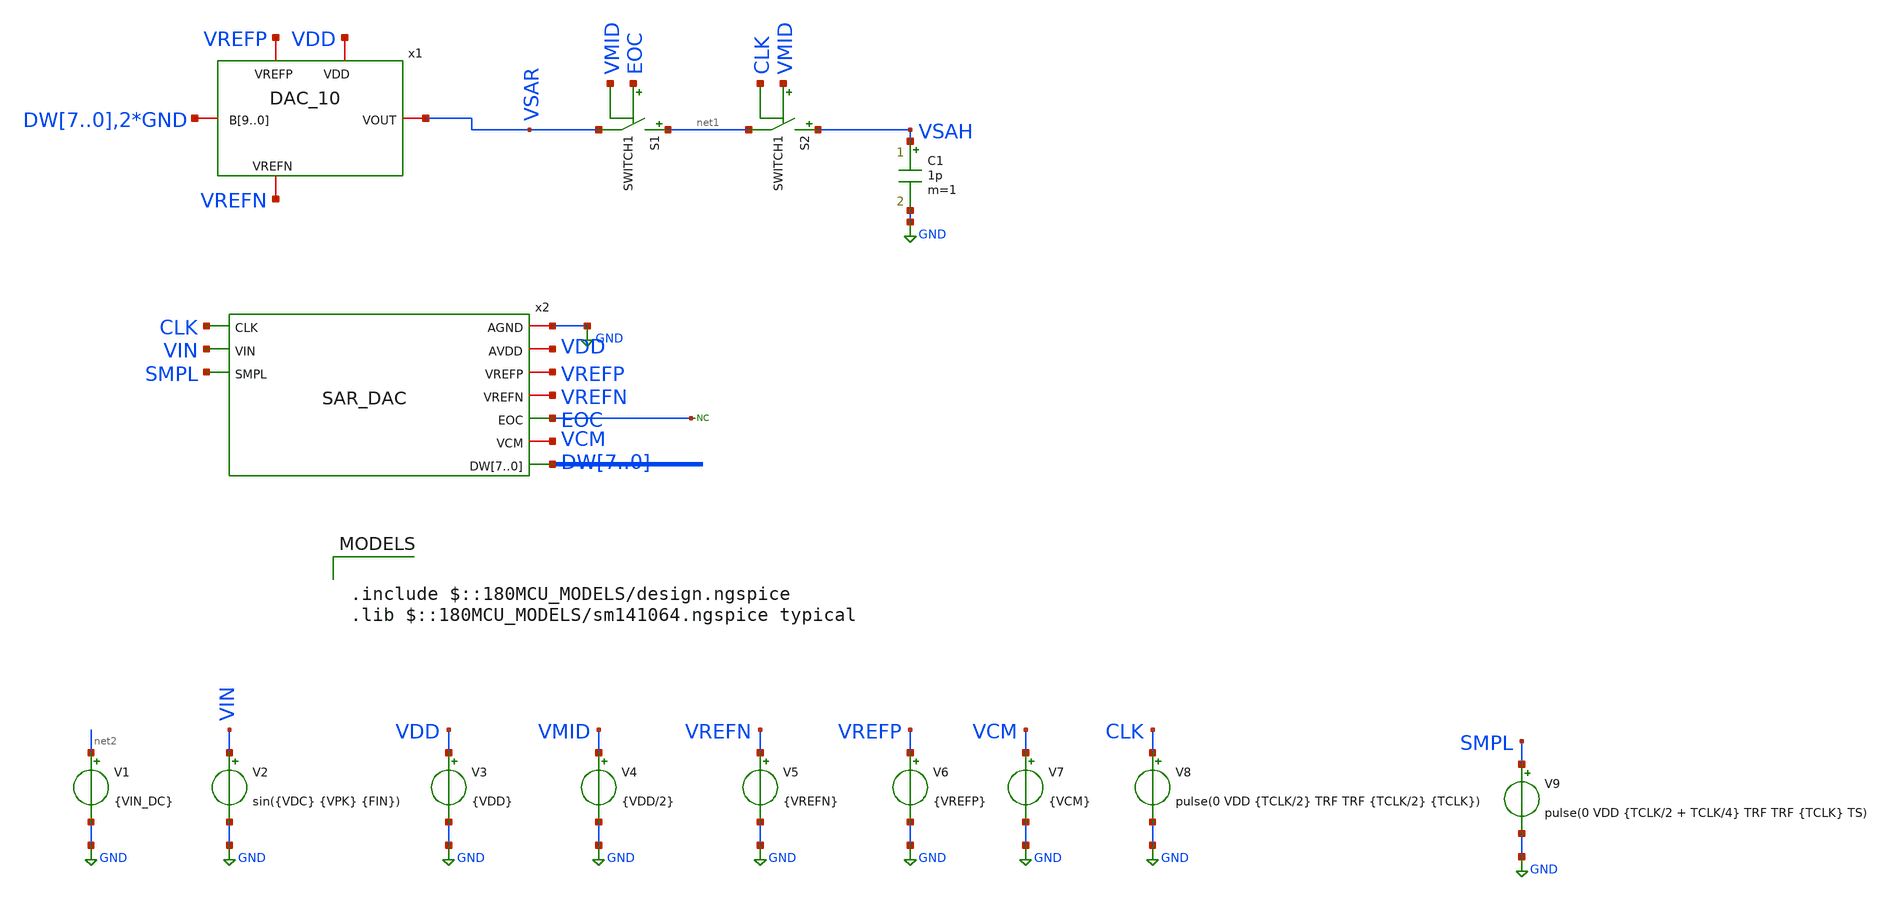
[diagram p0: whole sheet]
** sch_path: XSCHEM Files/final.sch
**.subckt final
S1 net1 VSAR EOC VMID SWITCH1
S2 VSAH net1 VMID CLK SWITCH1
C1 VSAH GND 1p m=1
V1 net2 GND {VIN_DC}
V2 VIN GND sin({VDC} {VPK} {FIN})
V3 VDD GND {VDD}
V4 VMID GND {VDD/2}
V5 VREFN GND {VREFN}
V6 VREFP GND {VREFP}
V7 VCM GND {VCM}
V8 CLK GND pulse(0 VDD {TCLK/2} TRF TRF {TCLK/2} {TCLK})
V9 SMPL GND pulse(0 VDD {TCLK/2 + TCLK/4} TRF TRF {TCLK} TS)
x1 VREFP VDD VSAR DW7 DW6 DW5 DW4 DW3 DW2 DW1 DW0 GND GND VREFN DAC_10
* noconn EOC
x2 GND VDD CLK VIN VREFP VREFN SMPL EOC VCM DW7 DW6 DW5 DW4 DW3 DW2 DW1 DW0 SAR_DAC
**** begin user architecture code

.include $::180MCU_MODELS/design.ngspice
.lib $::180MCU_MODELS/sm141064.ngspice typical



* ngspice commands
*Required model for the switch (the switch threshold default value is zero)
* you can define the threshold using vt={VDD/2} (not needed here)
.model SWITCH1 sw
*These are the values of the parameters to be used
.param TS=1u TCLK=100n TRF=1n TDROP={0.5/FIN} TSTOP={(NCYC/FIN)+TDROP}
.param NCYC=5 NFFT=256 FIN={(NCYC/NFFT)/TS}
.param VDD=3 VDC={1} VCM={1} VPK={0.5} VREFP={VCM+VPK} VREFN={VCM-VPK}
.param VCC=VDD
*.param VIN_DC={VREFN}
*.param VIN_DC={VREFP}
.param VIN_DC= {VREFN +(128+32+8+2+0.5)*2*VPK/(2**8)}
*Analysis setup and control statements
.tran 1n {TSTOP} {TDROP}
*.tran 1n {2*TS}
*save all voltages and currents
.save all
*options for an accurate precision output
*.options reltol=1e-6 vntol=1u abstol=1p
* option to make output file ascii
*.options filetype=ascii


**** end user architecture code
**.ends

* expanding   symbol:  /home/tare/Desktop/Final_1/DAC_10.sym # of pins=5
** sym_path: XSCHEM Files/DAC_10.sym
** sch_path: XSCHEM Files/DAC_10.sch
.subckt DAC_10 VREFP VDD VOUT B9 B8 B7 B6 B5 B4 B3 B2 B1 B0 VREFN
*.iopin B9,B8,B7,B6,B5,B4,B3,B2,B1,B0
*.iopin VREFP
*.iopin VREFN
*.iopin VOUT
*.iopin VDD
x19 VDD BO9 B9 Bitlogic
x18 VDD BO8 B8 Bitlogic
x17 VDD BO7 B7 Bitlogic
x16 VDD BO6 B6 Bitlogic
x15 VDD BO5 B5 Bitlogic
x14 VDD BO4 B4 Bitlogic
x13 VDD BO3 B3 Bitlogic
x12 VDD BO2 B2 Bitlogic
x11 VDD BO1 B1 Bitlogic
x10 VDD BO0 B0 Bitlogic
B1 VOUT GND
+ v=(512*v(BO9)+256*v(BO8)+128*v(BO7)+64*v(BO6)+32*v(BO5)+16*v(BO4)+8*v(BO3)+4*v(BO2)+2*v(BO1)+v(BO0))*((v(VREFP)-v(VREFN))/1024)+v(VREFN)
.ends


* expanding   symbol:  /home/tare/Desktop/last/SAR_DAC.sym # of pins=10
** sym_path: XSCHEM Files/SAR_DAC.sym
** sch_path: XSCHEM Files/SAR_DAC.sch
.subckt SAR_DAC AGND AVDD CLK VIN VREFP VREFN SMPL EOC VCM DW7 DW6 DW5 DW4 DW3 DW2 DW1 DW0
*.iopin AGND
*.iopin AVDD
*.iopin VREFP
*.iopin VREFN
*.iopin VCM
*.ipin VIN
*.ipin SMPL
*.ipin CLK
*.opin EOC
*.opin DW7,DW6,DW5,DW4,DW3,DW2,DW1,DW0
* noconn DW_B[7..0]
* noconn #net1
x8 CMP CLK SMPL DW7 DW6 DW5 DW4 DW3 DW2 DW1 DW0 DW_B7 DW_B6 DW_B5 DW_B4 DW_B3 DW_B2 DW_B1 DW_B0 EOC
+ sar_logic
x2 CMP VCM net1 VDAC comperator
x4 SMPL_B SMPL inv
x5 SMPL_D SMPL_B inv
x6 SMPL_B_D SMPL_D inv
x1 AVDD AGND VREFN VREFP SMPL_B_D DW7 DW6 DW5 DW4 DW3 DW2 DW1 DW0 SMPL_D VREFN VIN VDAC Cap_DAC
x3 SMPL AGND VDAC VCM AVDD tg
.ends


* expanding   symbol:  Bitlogic.sym # of pins=3
** sym_path: XSCHEM Files/Bitlogic.sym
** sch_path: XSCHEM Files/Bitlogic.sch
.subckt Bitlogic VDD BOUT BIN
*.opin BOUT
*.ipin BIN
*.iopin VDD
V1 ONE GND 1
S1 ONE BOUT BIN VMID SWITCH1
S2 BOUT GND VMID BIN SWITCH1
R1 VMID GND 1meg m=1
R2 VDD VMID 1meg m=1
.ends


* expanding   symbol:  /home/tare/Desktop/Final_1/sar_logic.sym # of pins=6
** sym_path: XSCHEM Files/sar_logic.sym
** sch_path: XSCHEM Files/sar_logic.sch
.subckt sar_logic CMP CLK RST DW7 DW6 DW5 DW4 DW3 DW2 DW1 DW0 DW_B7 DW_B6 DW_B5 DW_B4 DW_B3 DW_B2
+ DW_B1 DW_B0 EOC
*.ipin CMP
*.opin DW7,DW6,DW5,DW4,DW3,DW2,DW1,DW0
*.ipin CLK
*.ipin RST
*.opin DW_B7,DW_B6,DW_B5,DW_B4,DW_B3,DW_B2,DW_B1,DW_B0
*.opin EOC
**** begin user architecture code


V1 VLOW 0 0


**** end user architecture code
xRING_CNT8 VLOW CLK RST VLOW QCNT8 Q_B8 dff
xRING_CNT7 QCNT8 CLK VLOW RST QCNT7 Q_B7 dff
xRING_CNT6 QCNT7 CLK VLOW RST QCNT6 Q_B6 dff
xRING_CNT5 QCNT6 CLK VLOW RST QCNT5 Q_B5 dff
xRING_CNT4 QCNT5 CLK VLOW RST QCNT4 Q_B4 dff
xRING_CNT3 QCNT4 CLK VLOW RST QCNT3 Q_B3 dff
xRING_CNT2 QCNT3 CLK VLOW RST QCNT2 Q_B2 dff
xRING_CNT1 QCNT2 CLK VLOW RST QCNT1 Q_B1 dff
xRING_CNT0 QCNT1 CLK VLOW RST QCNT0 Q_B0 dff
xCODE_REG7 CMP DW6 QCNT8 VLOW DW7 DW_B7 dff
xCODE_REG6 CMP DW5 QCNT7 RST DW6 DW_B6 dff
xCODE_REG5 CMP DW4 QCNT6 RST DW5 DW_B5 dff
xCODE_REG4 CMP DW3 QCNT5 RST DW4 DW_B4 dff
xCODE_REG3 CMP DW2 QCNT4 RST DW3 DW_B3 dff
xCODE_REG2 CMP DW1 QCNT3 RST DW2 DW_B2 dff
xCODE_REG1 CMP DW0 QCNT2 RST DW1 DW_B1 dff
xCODE_REG0 CMP EOC QCNT1 RST DW0 DW_B0 dff
x3 VLOW VLOW QCNT0 RST EOC net1 dff
.ends


* expanding   symbol:  /home/tare/Desktop/Final_1/comperator.sym # of pins=4
** sym_path: XSCHEM Files/comperator.sym
** sch_path: XSCHEM Files/comperator.sch
.subckt comperator VOUTP VINP VOUTN VINN
*.ipin VINP
*.opin VOUTP
*.ipin VINN
*.opin VOUTN
V1 VINPi VINP 0
V2 VINNi VINN 0
B2 VOUTN GND V = {VCC/2 + VCC/2 *(tanh(V(VINPi,VINNi)*1e6*-1))}
B1 VOUTP GND V = {VCC/2 + VCC/2 *(tanh(V(VINPi,VINNi)*1e6))}
.ends


* expanding   symbol:  /home/tare/Desktop/Final_1/inv.sym # of pins=2
** sym_path: XSCHEM Files/inv.sym
** sch_path: XSCHEM Files/inv.sch
.subckt inv Y A
*.ipin A
*.opin Y
**** begin user architecture code


*inverter model
a1 A Yi my_inv
.model my_inv d_inverter(rise_delay = 1e-9 fall_delay = 1e-9                         input_load =
+ 1e-12)

*force netlisting of digital outputs
v1 Yi Y 0


**** end user architecture code
.ends


* expanding   symbol:  /home/tare/Desktop/last/Cap_DAC.sym # of pins=10
** sym_path: XSCHEM Files/Cap_DAC.sym
** sch_path: XSCHEM Files/Cap_DAC.sch
.subckt Cap_DAC AVDD AGND VREFN VREFP SMPL_B DW7 DW6 DW5 DW4 DW3 DW2 DW1 DW0 SMPL DW_D VIN VDAC
*.iopin AVDD
*.iopin VREFP
*.iopin VREFN
*.ipin VIN
*.ipin SMPL_B
*.ipin SMPL
*.opin VDAC
*.ipin DW7,DW6,DW5,DW4,DW3,DW2,DW1,DW0
*.ipin DW_D
*.iopin AGND
C0 VDAC VBOT_D 1f m=1
C1 VDAC VBOT0 1f m=1
C2 VDAC VBOT1 1f m=2
C3 VDAC VBOT2 1f m=4
C4 VDAC VBOT3 1f m=8
C5 VDAC VBOT4 1f m=16
C6 VDAC VBOT5 1f m=32
C7 VDAC VBOT6 1f m=64
C8 VDAC VBOT7 1f m=128
x17 VREFN VREFP AGND AVDD VIN DW7 SMPL SMPL_B VBOT7 Bottom_Plate
x16 VREFN VREFP AGND AVDD VIN DW6 SMPL SMPL_B VBOT6 Bottom_Plate
x15 VREFN VREFP AGND AVDD VIN DW5 SMPL SMPL_B VBOT5 Bottom_Plate
x14 VREFN VREFP AGND AVDD VIN DW4 SMPL SMPL_B VBOT4 Bottom_Plate
x13 VREFN VREFP AGND AVDD VIN DW3 SMPL SMPL_B VBOT3 Bottom_Plate
x12 VREFN VREFP AGND AVDD VIN DW2 SMPL SMPL_B VBOT2 Bottom_Plate
x11 VREFN VREFP AGND AVDD VIN DW1 SMPL SMPL_B VBOT1 Bottom_Plate
x10 VREFN VREFP AGND AVDD VIN DW0 SMPL SMPL_B VBOT0 Bottom_Plate
x2 VREFN VREFP AGND AVDD VIN DW_D SMPL SMPL_B VBOT_D Bottom_Plate
.ends


* expanding   symbol:  /home/tare/Desktop/last/tg.sym # of pins=5
** sym_path: XSCHEM Files/tg.sym
** sch_path: XSCHEM Files/tg.sch
.subckt tg EN AGND VOUT VIN AVDD
*.iopin AGND
*.iopin AVDD
*.iopin VOUT
*.iopin VIN
*.iopin EN
XM1 VOUT EN VIN AGND nmos_3p3 L=0.28u W=5u nf=1 ad='int((nf+1)/2) * W/nf * 0.18u' as='int((nf+2)/2) * W/nf * 0.18u'
+ pd='2*int((nf+1)/2) * (W/nf + 0.18u)' ps='2*int((nf+2)/2) * (W/nf + 0.18u)' nrd='0.18u / W' nrs='0.18u / W'
+ sa=0 sb=0 sd=0 m=1
XM2 VOUT ENB VIN AVDD pmos_3p3 L=0.28u W=10u nf=1 ad='int((nf+1)/2) * W/nf * 0.18u' as='int((nf+2)/2) * W/nf * 0.18u'
+ pd='2*int((nf+1)/2) * (W/nf + 0.18u)' ps='2*int((nf+2)/2) * (W/nf + 0.18u)' nrd='0.18u / W' nrs='0.18u / W'
+ sa=0 sb=0 sd=0 m=1
E1 ENB AVDD EN AGND -1
.ends


* expanding   symbol:  /home/tare/Desktop/sar_adc/dff.sym # of pins=6
** sym_path: XSCHEM Files/dff.sym
** sch_path: XSCHEM Files/dff.sch
.subckt dff D CLK SET RESET Q QB
*.ipin D
*.opin Q
*.ipin CLK
*.ipin SET
*.ipin RESET
*.opin QB
**** begin user architecture code


*nor model
a1 D CLK SET RESET OUT OUTI my_dff
.model my_dff d_dff(clk_delay = 13.0e-9 set_delay = 25.0e-9                    reset_delay = 27.0e-9
+ ic = 2 rise_delay = 10.0e-9                    fall_delay = 3e-9)

*force netlisting of digital outputs
v1 OUT Q 0
v2 OUTI QB 1


**** end user architecture code
.ends


* expanding   symbol:  /home/tare/Desktop/last/Bottom_Plate.sym # of pins=9
** sym_path: XSCHEM Files/Bottom_Plate.sym
** sch_path: XSCHEM Files/Bottom_Plate.sch
.subckt Bottom_Plate VREFN VREFP AGND AVDD VIN D SMPL SMPL_B VBOT
*.iopin AGND
*.iopin AVDD
*.iopin VREFP
*.iopin VREFN
*.opin VBOT
*.ipin VIN
*.ipin D
*.ipin SMPL_B
*.ipin SMPL
XM1 VBOT net1 VREFN AGND nmos_3p3 L=0.28u W=5u nf=1 ad='int((nf+1)/2) * W/nf * 0.18u' as='int((nf+2)/2) * W/nf * 0.18u'
+ pd='2*int((nf+1)/2) * (W/nf + 0.18u)' ps='2*int((nf+2)/2) * (W/nf + 0.18u)' nrd='0.18u / W' nrs='0.18u / W'
+ sa=0 sb=0 sd=0 m=1
XM2 VREFP net2 VBOT AVDD pmos_3p3 L=0.28u W=10u nf=1 ad='int((nf+1)/2) * W/nf * 0.18u' as='int((nf+2)/2) * W/nf * 0.18u'
+ pd='2*int((nf+1)/2) * (W/nf + 0.18u)' ps='2*int((nf+2)/2) * (W/nf + 0.18u)' nrd='0.18u / W' nrs='0.18u / W'
+ sa=0 sb=0 sd=0 m=1
x2 net1 D SMPL nor
x3 net2 D SMPL_B nand
x1 SMPL AGND VBOT VIN AVDD tg
.ends


* expanding   symbol:  /home/tare/Desktop/Final_1/nor.sym # of pins=3
** sym_path: XSCHEM Files/nor.sym
** sch_path: XSCHEM Files/nor.sch
.subckt nor Y A B
*.ipin A
*.opin Y
*.ipin B
**** begin user architecture code


*nor model
a1 [A b] Yi my_nor
.model my_nor d_nor(rise_delay = 1e-9 fall_delay = 1e-9                         input_load = 1e-12)

*force netlisting of digital outputs
v1 Yi Y 0


**** end user architecture code
.ends


* expanding   symbol:  /home/tare/Desktop/Final_1/nand.sym # of pins=3
** sym_path: XSCHEM Files/nand.sym
** sch_path: XSCHEM Files/nand.sch
.subckt nand Y A B
*.ipin A
*.opin Y
*.ipin B
**** begin user architecture code


*nand model
a1 [A b] Yi my_nand
.model my_nand d_nand(rise_delay = 1e-9 fall_delay = 1e-9                         input_load =
+ 1e-12)

*force netlisting of digital outputs
v1 Yi Y 0


**** end user architecture code
.ends

.GLOBAL GND
.end
